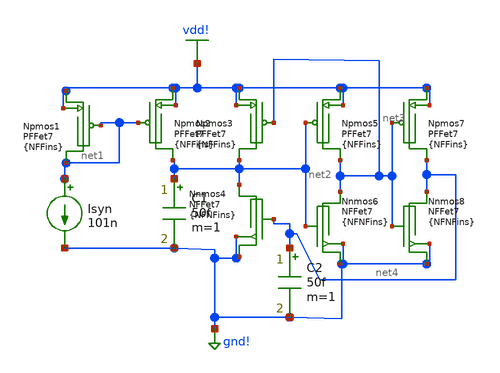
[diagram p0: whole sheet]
** sch_path: SimulationModeling/BesrourOptimal.sch
**.subckt BesrourOptimal
Npmos2 vdd! net1 net2 vdd! BSIMCMG_osdi_P nfin={NFFins}
Npmos5 vdd! net2 net3 vdd! BSIMCMG_osdi_P nfin={NFFins}
Npmos7 vdd! net3 net4 vdd! BSIMCMG_osdi_P nfin={NFFins}
Nnmos6 gnd! net2 net3 gnd! BSIMCMG_osdi_N nfin={NFNFins}
Nnmos8 gnd! net3 net4 gnd! BSIMCMG_osdi_N nfin={NFNFins}
C2 net4 gnd! 50f m=1
C1 net2 gnd! 50f m=1
Npmos1 vdd! net1 net1 vdd! BSIMCMG_osdi_P nfin={NFFins}
Npmos3 vdd! net3 net2 vdd! BSIMCMG_osdi_P nfin={NFFins}
Nnmos4 gnd! net4 net2 gnd! BSIMCMG_osdi_N nfin={NFNFins}
Isyn net1 gnd! 101n
**** begin user architecture code



* ngspice commands
.include asap7_TT_slvt.sp
.param NFFins=1
.param NFNFins=5
* Power supplies
Vvdd vdd! 0 dc=0.7
Vgnd gnd! 0 dc=0
* Initial conditions
.ic v(net2)=0 v(net4)=0
.control
    * Reduce maximum timestep
    set maxstep = 0.01n

    * Add integration method controls
    set method = gear
    set gmin = 1e-15

    * Increase iteration limits
    set itl1 = 1000
    set itl4 = 1000
    set num_threads = 24
    set parallel = 1
    set filetype=ascii
    set wr_vecnames
    set wr_singlescale

    * Create output file in current directory
    echo VDD Cap1 Cap2 Spikes Frequency Energy_Per_Spike > /Users/logan/Desktop/besourneuron.txt

    alter Isyn = 100n

    let vdd_start = 0.1
    let vdd_stop = 0.91
    let vdd_step = 0.01
    let vdd = $&vdd_start

    while vdd <= $&vdd_stop
        alter Vvdd dc=$&vdd
        let vth = 0.2 * $&vdd
        let low_th = 0.05 * $&vdd

        foreach cap1 0.69e-15
            alter C1 = $cap1

            foreach cap2 0.2e-15
                alter C2 = $cap2

                tran 0.04n 1u UIC

                let power_vdd = -1*v(vdd!)*i(Vvdd)
                let dt = time[1] - time[0]

                let transitions = vector(length(v(net4)))
                let i = 0
                let count = 0
                let last_state = 0
                let spike_energy = 0
                let current_spike_energy = 0

                dowhile i < length(v(net4))-1
                    if (v(net4)[i] gt $&vth and last_state eq 0)
                        let count = count + 1
                        let last_state = 1
                        let current_spike_energy = 0
                    end
                    if (last_state eq 1)
                        let current_spike_energy = current_spike_energy + power_vdd[i] * $&dt
                    end
                    if (v(net4)[i] lt $&low_th)
                        if (last_state eq 1)
                            let spike_energy = spike_energy + current_spike_energy
                        end
                        let last_state = 0
                    end
                    let i = i + 1
                end

                let spike_count = $&count
                let sim_time = 1e-6
                let spiking_freq = $&spike_count / sim_time
                let energy_per_spike = 0
                if spike_count gt 0
                    let energy_per_spike = (spike_energy / spike_count)
                end

                * Write to file and also echo to screen
                echo $&vdd $cap1 $cap2 $&spike_count $&spiking_freq $&energy_per_spike >>
+ /Users/logan/Desktop/besourneuron.txt
                echo At VDD=$&vdd V Cap1=$cap1 F Cap2=$cap2 F Spikes=$&spike_count Spikes
+ Freq=$&spiking_freq Hz Energy/Spike=$&energy_per_spike J
            end
        end
        let vdd = vdd + $&vdd_step
    end
.endc



**** end user architecture code
**.ends
.GLOBAL vdd!
.GLOBAL gnd!
.end
